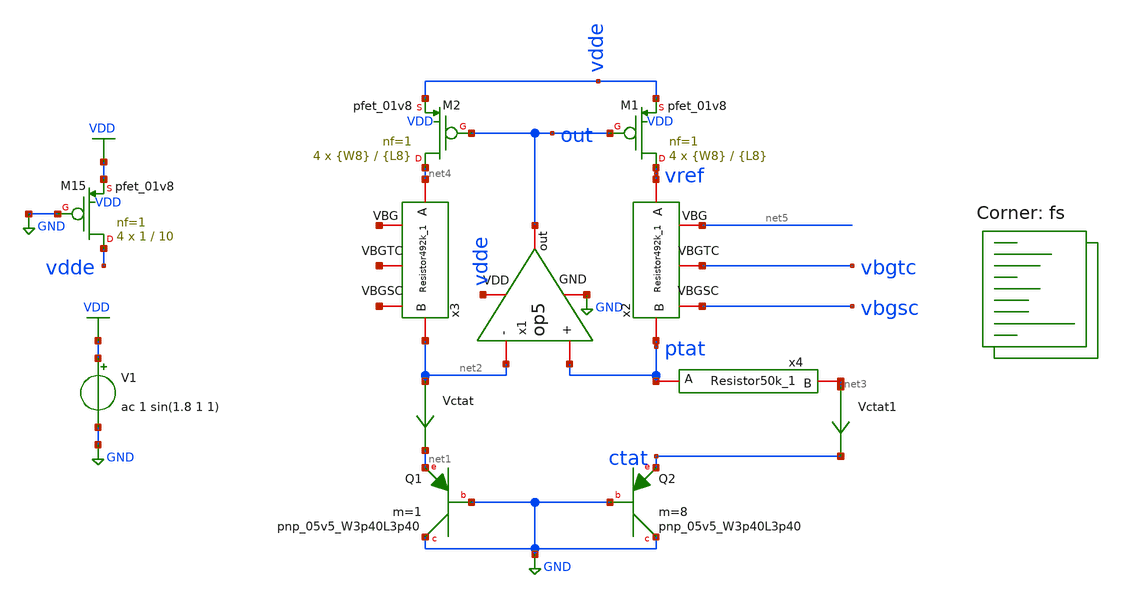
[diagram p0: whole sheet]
** sch_path: xschem/bgr_op5_vref.sch
**.subckt bgr_op5_vref
XQ1 GND GND net1 sky130_fd_pr__pnp_05v5_W3p40L3p40 m=1
XQ2 GND GND ctat sky130_fd_pr__pnp_05v5_W3p40L3p40 m=8
Vctat net2 net1 0
.save i(vctat)
V1 VDD GND ac 1 sin(1.8 1 1)
XM1 vref out vdde VDD sky130_fd_pr__pfet_01v8 L={L8} W={W8} nf=1 ad='int((nf+1)/2) * W/nf * 0.29' as='int((nf+2)/2) * W/nf * 0.29'
+ pd='2*int((nf+1)/2) * (W/nf + 0.29)' ps='2*int((nf+2)/2) * (W/nf + 0.29)' nrd='0.29 / W' nrs='0.29 / W'
+ sa=0 sb=0 sd=0 mult=4 m=4
XM2 net4 out vdde VDD sky130_fd_pr__pfet_01v8 L={L8} W={W8} nf=1 ad='int((nf+1)/2) * W/nf * 0.29' as='int((nf+2)/2) * W/nf * 0.29'
+ pd='2*int((nf+1)/2) * (W/nf + 0.29)' ps='2*int((nf+2)/2) * (W/nf + 0.29)' nrd='0.29 / W' nrs='0.29 / W'
+ sa=0 sb=0 sd=0 mult=4 m=4
x1 vdde out net2 ptat GND op5
XM15 vdde GND VDD VDD sky130_fd_pr__pfet_01v8 L=10 W=1 nf=1 ad='int((nf+1)/2) * W/nf * 0.29' as='int((nf+2)/2) * W/nf * 0.29'
+ pd='2*int((nf+1)/2) * (W/nf + 0.29)' ps='2*int((nf+2)/2) * (W/nf + 0.29)' nrd='0.29 / W' nrs='0.29 / W'
+ sa=0 sb=0 sd=0 mult=4 m=4
Vctat1 net3 ctat 0
.save i(vctat1)
x2 net5 vref ptat vbgtc vbgsc Resistor492k_1
x3 net6 net4 net2 net7 net8 Resistor492k_1
x4 net3 ptat Resistor50k_1
**** begin user architecture code


.param L8=10
.param W8=1
.param L10=1
.param W10=1
.param R=492k




.option savecurrents
.control
save all
op
remzerovec
*write bgr_op5.raw
set appendwrite
set wr_singlescale
set wr_vecnames
option numdgt=3

dc temp -40 85 1
remzerovec
*write VREFFS.raw vref
*plot (ptat-ctat)
*plot ctat
plot vref
*wrdata vref5.csv vref
*plot vbgsc vbgtc

********TC********
meas dc temp_avg_vref avg v(vref)
meas dc temp_vref_27 find v(vref) when temp-sweep=27
meas dc temp_pp_vref PP v(vref)
meas dc temp_vref_max max v(vref)
meas dc temp_max_vref when v(vref)='temp_vref_max'
meas dc temp_vref_min min v(vref)
meas dc temp_min_vref when v(vref)='temp_vref_min'
let vref_tc='((temp_pp_vref*1000000)/(125*temp_avg_vref))'
print vref_tc

******PSRR******
ac dec 1000 1 10Meg
write PSRRFS.raw vdb(vref)
remzerovec
plot vdb(vref)
*wrdata PSRR5.csv vdb(vref)
meas ac psrr find vdb(vref) at=1k

****Power****
tran 10ms 500ms
*write bgr_op5.raw
set altshow
show >> bgr_op5.lis
remzerovec
meas tran ave_v avg vdd
meas tran ave_i avg i(v1)
let ave_power='ave_v*(-ave_i)
plot vdd vref
*plot -i(v1)
print ave_power

*******LS******
dc v1 0 3.5 0.1
write bgr_op5.raw
remzerovec
plot vdd vref
meas dc vbg_27 find v(vref) at=1.8
meas dc vbgsc_27 find v(vbgsc) at=1.8
meas dc vbgtc_27 find v(vbgtc) at=1.8
meas dc vref_max max v(vref) from=1.62 to=1.98
meas dc vref_min min v(vref) from=1.62 to=1.98
let ls='(vref_max-vref_min)/(1.98-1.62)'
print ls

.endc


.lib $::SKYWATER_MODELS/sky130.lib.spice fs
**** end user architecture code
**.ends

* expanding   symbol:  op5.sym # of pins=5
** sym_path: xschem/op5.sym
** sch_path: xschem/op5.sch
.subckt op5 VDD out - + GND
*.iopin VDD
*.iopin GND
*.iopin -
*.iopin +
*.iopin out
C2 out net5 2.2p m=1
R2 net5 net1 1k m=1
XM1 bias bias net6 GND sky130_fd_pr__nfet_01v8 L={L5} W={W5} nf=1 ad='int((nf+1)/2) * W/nf * 0.29' as='int((nf+2)/2)
+ * W/nf * 0.29' pd='2*int((nf+1)/2) * (W/nf + 0.29)' ps='2*int((nf+2)/2) * (W/nf + 0.29)' nrd='0.29 /
+ W' nrs='0.29 / W' sa=0 sb=0 sd=0 mult=4 m=4
XM2 net4 bias GND GND sky130_fd_pr__nfet_01v8 L={L5} W={W5} nf=1 ad='int((nf+1)/2) * W/nf * 0.29' as='int((nf+2)/2)
+ * W/nf * 0.29' pd='2*int((nf+1)/2) * (W/nf + 0.29)' ps='2*int((nf+2)/2) * (W/nf + 0.29)' nrd='0.29 /
+ W' nrs='0.29 / W' sa=0 sb=0 sd=0 mult=4 m=4
XM3 net2 - net3 GND sky130_fd_pr__nfet_01v8 L={L4} W={W4} nf=1 ad='int((nf+1)/2) * W/nf * 0.29' as='int((nf+2)/2)
+ * W/nf * 0.29' pd='2*int((nf+1)/2) * (W/nf + 0.29)' ps='2*int((nf+2)/2) * (W/nf + 0.29)' nrd='0.29 /
+ W' nrs='0.29 / W' sa=0 sb=0 sd=0 mult=4 m=4
XM4 net1 + net3 GND sky130_fd_pr__nfet_01v8 L={L4} W={W4} nf=1 ad='int((nf+1)/2) * W/nf * 0.29' as='int((nf+2)/2)
+ * W/nf * 0.29' pd='2*int((nf+1)/2) * (W/nf + 0.29)' ps='2*int((nf+2)/2) * (W/nf + 0.29)' nrd='0.29 /
+ W' nrs='0.29 / W' sa=0 sb=0 sd=0 mult=4 m=4
XM6 bias net4 VDD VDD sky130_fd_pr__pfet_01v8 L={L1} W={W1} nf=1 ad='int((nf+1)/2) * W/nf * 0.29' as='int((nf+2)/2)
+ * W/nf * 0.29' pd='2*int((nf+1)/2) * (W/nf + 0.29)' ps='2*int((nf+2)/2) * (W/nf + 0.29)' nrd='0.29 /
+ W' nrs='0.29 / W' sa=0 sb=0 sd=0 mult=4 m=4
XM7 net4 net4 VDD VDD sky130_fd_pr__pfet_01v8 L={L1} W={W1} nf=1 ad='int((nf+1)/2) * W/nf * 0.29' as='int((nf+2)/2)
+ * W/nf * 0.29' pd='2*int((nf+1)/2) * (W/nf + 0.29)' ps='2*int((nf+2)/2) * (W/nf + 0.29)' nrd='0.29 /
+ W' nrs='0.29 / W' sa=0 sb=0 sd=0 mult=4 m=4
XM8 net1 net2 VDD VDD sky130_fd_pr__pfet_01v8 L={L7} W={W7} nf=1 ad='int((nf+1)/2) * W/nf * 0.29' as='int((nf+2)/2)
+ * W/nf * 0.29' pd='2*int((nf+1)/2) * (W/nf + 0.29)' ps='2*int((nf+2)/2) * (W/nf + 0.29)' nrd='0.29 /
+ W' nrs='0.29 / W' sa=0 sb=0 sd=0 mult=4 m=4
XM9 net2 net2 VDD VDD sky130_fd_pr__pfet_01v8 L={L7} W={W7} nf=1 ad='int((nf+1)/2) * W/nf * 0.29' as='int((nf+2)/2)
+ * W/nf * 0.29' pd='2*int((nf+1)/2) * (W/nf + 0.29)' ps='2*int((nf+2)/2) * (W/nf + 0.29)' nrd='0.29 /
+ W' nrs='0.29 / W' sa=0 sb=0 sd=0 mult=4 m=4
XM5 net3 bias GND GND sky130_fd_pr__nfet_01v8 L={L6} W={W6} nf=1 ad='int((nf+1)/2) * W/nf * 0.29' as='int((nf+2)/2)
+ * W/nf * 0.29' pd='2*int((nf+1)/2) * (W/nf + 0.29)' ps='2*int((nf+2)/2) * (W/nf + 0.29)' nrd='0.29 /
+ W' nrs='0.29 / W' sa=0 sb=0 sd=0 mult=4 m=4
XM10 out net1 VDD VDD sky130_fd_pr__pfet_01v8 L={L2} W={W2} nf=1 ad='int((nf+1)/2) * W/nf * 0.29' as='int((nf+2)/2)
+ * W/nf * 0.29' pd='2*int((nf+1)/2) * (W/nf + 0.29)' ps='2*int((nf+2)/2) * (W/nf + 0.29)' nrd='0.29 /
+ W' nrs='0.29 / W' sa=0 sb=0 sd=0 mult=4 m=4
XM11 out bias GND GND sky130_fd_pr__nfet_01v8 L={L3} W={W3} nf=1 ad='int((nf+1)/2) * W/nf * 0.29' as='int((nf+2)/2)
+ * W/nf * 0.29' pd='2*int((nf+1)/2) * (W/nf + 0.29)' ps='2*int((nf+2)/2) * (W/nf + 0.29)' nrd='0.29 /
+ W' nrs='0.29 / W' sa=0 sb=0 sd=0 mult=4 m=4
R3 net6 GND 5k m=1
**** begin user architecture code


**************
*PMOS cms
.param L1=2.7
.param W1=1.25

**************
*NMOS cms
.param L5=2
.param W5=3.5

**************
*PMOS current differential
.param L7=2.7
.param W7=1.25

**************
*differential Pair
.param L4=2.7
.param W4=1.25

**************
*NMOS current control
.param L6=2
.param W6=3.5

**************
*Second Stage
.param L2=2
.param W2=3.5

**************
*NMOS current second stage
.param L3=2
.param W3=3.5


**** end user architecture code
.ends


* expanding   symbol:  Resistor492k_1.sym # of pins=5
** sym_path: xschem/Resistor492k_1.sym
** sch_path: xschem/Resistor492k_1.sch
.subckt Resistor492k_1 VBG A B VBGTC VBGSC
*.iopin A
*.iopin VBGTC
*.iopin B
*.iopin VBGSC
*.iopin VBG
XR1 net1 A GND sky130_fd_pr__res_high_po_0p35 L={L} mult=1 m=1
XR2 net2 net1 GND sky130_fd_pr__res_high_po_0p35 L={L} mult=1 m=1
XR3 VBG net2 GND sky130_fd_pr__res_high_po_0p35 L={L} mult=1 m=1
XR4 net3 VBG GND sky130_fd_pr__res_high_po_0p35 L={L} mult=1 m=1
XR5 net4 net3 GND sky130_fd_pr__res_high_po_0p35 L={L} mult=1 m=1
**** begin user architecture code


.param L=17


**** end user architecture code
XR6 net5 net6 GND sky130_fd_pr__res_high_po_0p35 L={L} mult=1 m=1
XR7 VBGSC net5 GND sky130_fd_pr__res_high_po_0p35 L={L} mult=1 m=1
XR8 VBGTC VBGSC GND sky130_fd_pr__res_high_po_0p35 L={L} mult=1 m=1
XR9 net7 VBGTC GND sky130_fd_pr__res_high_po_0p35 L={L} mult=1 m=1
XR10 net4 net7 GND sky130_fd_pr__res_high_po_0p35 L={L} mult=1 m=1
XR11 net8 net6 GND sky130_fd_pr__res_high_po_0p35 L={L} mult=1 m=1
XR12 net9 net8 GND sky130_fd_pr__res_high_po_0p35 L={L} mult=1 m=1
XR13 net11 net9 GND sky130_fd_pr__res_high_po_0p35 L={L} mult=1 m=1
XR14 net10 net11 GND sky130_fd_pr__res_high_po_0p35 L={L} mult=1 m=1
XR15 net12 net10 GND sky130_fd_pr__res_high_po_0p35 L={L} mult=1 m=1
XR16 net13 net14 GND sky130_fd_pr__res_high_po_0p35 L={L} mult=1 m=1
XR17 net15 net13 GND sky130_fd_pr__res_high_po_0p35 L={L} mult=1 m=1
XR18 net17 net15 GND sky130_fd_pr__res_high_po_0p35 L={L} mult=1 m=1
XR19 net16 net17 GND sky130_fd_pr__res_high_po_0p35 L={L} mult=1 m=1
XR20 net12 net16 GND sky130_fd_pr__res_high_po_0p35 L={L} mult=1 m=1
XR21 net18 net14 GND sky130_fd_pr__res_high_po_0p35 L={L} mult=1 m=1
XR22 B net18 GND sky130_fd_pr__res_high_po_0p35 L={L} mult=1 m=1
.ends


* expanding   symbol:  Resistor50k_1.sym # of pins=2
** sym_path: xschem/Resistor50k_1.sym
** sch_path: xschem/Resistor50k_1.sch
.subckt Resistor50k_1 B A
*.iopin A
*.iopin B
XR2 net2 net1 GND sky130_fd_pr__res_high_po_0p35 L={L} mult=1 m=1
**** begin user architecture code


.param L=17
.param La=8.5
.param L1=1
.param W1=15


**** end user architecture code
XR3 A net2 GND sky130_fd_pr__res_high_po_0p35 L={L} mult=1 m=1
XR1 net1 net3 GND sky130_fd_pr__res_high_po_0p35 L={La} mult=2 m=2
XR4 net3 net4 GND sky130_fd_pr__res_high_po_0p35 L={La} mult=4 m=4
XR5 net4 net5 GND sky130_fd_pr__res_high_po_0p35 L={La} mult=8 m=8
XR6 net5 B GND sky130_fd_pr__res_high_po_0p35 L={La} mult=16 m=16
V1 net6 GND 1.8
XM4 net1 net6 net3 GND sky130_fd_pr__nfet_01v8_lvt L={L1} W={W1} nf=1 ad='int((nf+1)/2) * W/nf * 0.29' as='int((nf+2)/2)
+ * W/nf * 0.29' pd='2*int((nf+1)/2) * (W/nf + 0.29)' ps='2*int((nf+2)/2) * (W/nf + 0.29)' nrd='0.29 /
+ W' nrs='0.29 / W' sa=0 sb=0 sd=0 mult=1 m=1
XM1 net3 GND net4 GND sky130_fd_pr__nfet_01v8_lvt L={L1} W={W1} nf=1 ad='int((nf+1)/2) * W/nf * 0.29' as='int((nf+2)/2)
+ * W/nf * 0.29' pd='2*int((nf+1)/2) * (W/nf + 0.29)' ps='2*int((nf+2)/2) * (W/nf + 0.29)' nrd='0.29 /
+ W' nrs='0.29 / W' sa=0 sb=0 sd=0 mult=1 m=1
XM2 net4 GND net5 GND sky130_fd_pr__nfet_01v8_lvt L={L1} W={W1} nf=1 ad='int((nf+1)/2) * W/nf * 0.29' as='int((nf+2)/2)
+ * W/nf * 0.29' pd='2*int((nf+1)/2) * (W/nf + 0.29)' ps='2*int((nf+2)/2) * (W/nf + 0.29)' nrd='0.29 /
+ W' nrs='0.29 / W' sa=0 sb=0 sd=0 mult=1 m=1
XM3 net5 GND B GND sky130_fd_pr__nfet_01v8_lvt L={L1} W={W1} nf=1 ad='int((nf+1)/2) * W/nf * 0.29' as='int((nf+2)/2)
+ * W/nf * 0.29' pd='2*int((nf+1)/2) * (W/nf + 0.29)' ps='2*int((nf+2)/2) * (W/nf + 0.29)' nrd='0.29 /
+ W' nrs='0.29 / W' sa=0 sb=0 sd=0 mult=1 m=1
.ends

.GLOBAL GND
.GLOBAL VDD
.end
